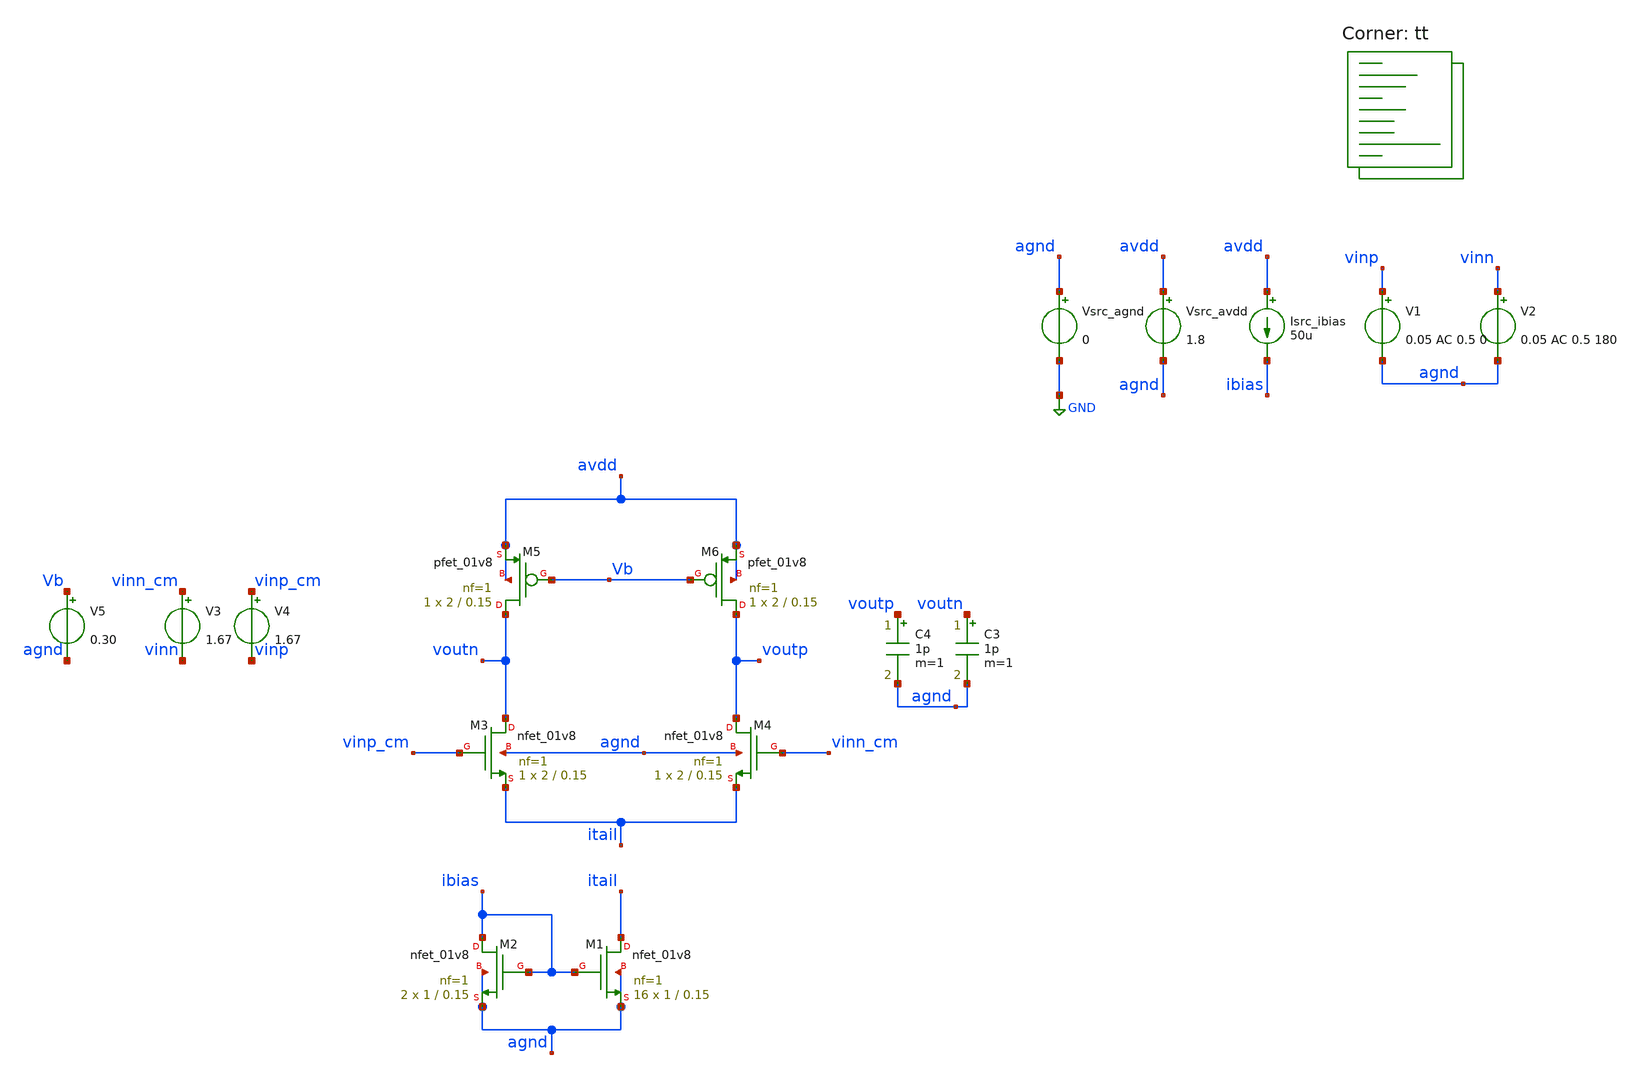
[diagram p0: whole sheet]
** sch_path: AMP/TB_Topologies_Diff.sch
**.subckt TB_Topologies_Diff
Vsrc_agnd agnd GND 0
Vsrc_avdd avdd agnd 1.8
Isrc_ibias avdd ibias 50u
V1 vinp agnd 0.05 AC 0.5 0
V2 vinn agnd 0.05 AC 0.5 180
C3 voutn agnd 1p m=1
C4 voutp agnd 1p m=1
XM1 itail ibias agnd agnd sky130_fd_pr__nfet_01v8 L=0.15 W=1 nf=1 ad='int((nf+1)/2) * W/nf * 0.29' as='int((nf+2)/2) * W/nf * 0.29'
+ pd='2*int((nf+1)/2) * (W/nf + 0.29)' ps='2*int((nf+2)/2) * (W/nf + 0.29)' nrd='0.29 / W' nrs='0.29 / W'
+ sa=0 sb=0 sd=0 mult=16 m=16
XM2 ibias ibias agnd agnd sky130_fd_pr__nfet_01v8 L=0.15 W=1 nf=1 ad='int((nf+1)/2) * W/nf * 0.29' as='int((nf+2)/2) * W/nf * 0.29'
+ pd='2*int((nf+1)/2) * (W/nf + 0.29)' ps='2*int((nf+2)/2) * (W/nf + 0.29)' nrd='0.29 / W' nrs='0.29 / W'
+ sa=0 sb=0 sd=0 mult=2 m=2
XM3 voutn vinp_cm itail agnd sky130_fd_pr__nfet_01v8 L=0.15 W=2 nf=1 ad='int((nf+1)/2) * W/nf * 0.29'
+ as='int((nf+2)/2) * W/nf * 0.29' pd='2*int((nf+1)/2) * (W/nf + 0.29)' ps='2*int((nf+2)/2) * (W/nf + 0.29)'
+ nrd='0.29 / W' nrs='0.29 / W' sa=0 sb=0 sd=0 mult=1 m=1
XM4 voutp vinn_cm itail agnd sky130_fd_pr__nfet_01v8 L=0.15 W=2 nf=1 ad='int((nf+1)/2) * W/nf * 0.29'
+ as='int((nf+2)/2) * W/nf * 0.29' pd='2*int((nf+1)/2) * (W/nf + 0.29)' ps='2*int((nf+2)/2) * (W/nf + 0.29)'
+ nrd='0.29 / W' nrs='0.29 / W' sa=0 sb=0 sd=0 mult=1 m=1
XM5 voutn Vb avdd avdd sky130_fd_pr__pfet_01v8 L=0.15 W=2 nf=1 ad='int((nf+1)/2) * W/nf * 0.29' as='int((nf+2)/2) * W/nf * 0.29'
+ pd='2*int((nf+1)/2) * (W/nf + 0.29)' ps='2*int((nf+2)/2) * (W/nf + 0.29)' nrd='0.29 / W' nrs='0.29 / W'
+ sa=0 sb=0 sd=0 mult=1 m=1
XM6 voutp Vb avdd avdd sky130_fd_pr__pfet_01v8 L=0.15 W=2 nf=1 ad='int((nf+1)/2) * W/nf * 0.29' as='int((nf+2)/2) * W/nf * 0.29'
+ pd='2*int((nf+1)/2) * (W/nf + 0.29)' ps='2*int((nf+2)/2) * (W/nf + 0.29)' nrd='0.29 / W' nrs='0.29 / W'
+ sa=0 sb=0 sd=0 mult=1 m=1
V3 vinn_cm vinn 1.67
V4 vinp_cm vinp 1.67
V5 Vb agnd 0.30
**** begin user architecture code

* this option enables mos model bin
* selection based on W/NF instead of W
.option wnflag=1

.option savecurrents

.control
save all
op

* Print newline
echo

* Store MOS lists
set nmos_list = ( xm1 xm2 xm3 xm4 )
set pmos_list = ( xm5 xm6 )
set nmos_lvt_list = (  )
set pmos_lvt_list = (  )

* Print stats for each MOSFET
foreach nmos $nmos_list
 * Save stats
 save @m.{$nmos}.msky130_fd_pr__nfet_01v8[gm]
 let vth   = @m.{$nmos}.msky130_fd_pr__nfet_01v8[vth]
 let vgs   = @m.{$nmos}.msky130_fd_pr__nfet_01v8[vgs]
 let vds   = @m.{$nmos}.msky130_fd_pr__nfet_01v8[vds]
 let vdsat = @m.{$nmos}.msky130_fd_pr__nfet_01v8[vdsat]
 let gm    = @m.{$nmos}.msky130_fd_pr__nfet_01v8[gm]
 let gds   = @m.{$nmos}.msky130_fd_pr__nfet_01v8[gds]


 * Print stats
 echo Stats for $nmos:
 print vth
 print vgs
 print vds
 print vdsat
 print gm
 print gds

 * Print newline
 echo
end

foreach pmos $pmos_list
 * Save stats
 save @m.{$pmos}.msky130_fd_pr__nfet_01v8[gm]
 let vth   = @m.{$pmos}.msky130_fd_pr__pfet_01v8[vth]
 let vgs   = @m.{$pmos}.msky130_fd_pr__pfet_01v8[vgs]
 let vds   = @m.{$pmos}.msky130_fd_pr__pfet_01v8[vds]
 let vdsat = @m.{$pmos}.msky130_fd_pr__pfet_01v8[vdsat]
 let gm    = @m.{$pmos}.msky130_fd_pr__pfet_01v8[gm]
 let gds   = @m.{$pmos}.msky130_fd_pr__pfet_01v8[gds]

 * Print stats
 echo Stats for $pmos:
 print vth
 print vgs
 print vds
 print vdsat
 print gm
 print gds

 * Print newline
 echo
end

foreach nmos_lvt $nmos_lvt_list
 * Save stats
 save @m.{$nmos_lvt}.msky130_fd_pr__nfet_01v8_lvt[gm]
 let vth   = @m.{$nmos_lvt}.msky130_fd_pr__nfet_01v8_lvt[vth]
 let vgs   = @m.{$nmos_lvt}.msky130_fd_pr__nfet_01v8_lvt[vgs]
 let vds   = @m.{$nmos_lvt}.msky130_fd_pr__nfet_01v8_lvt[vds]
 let vdsat = @m.{$nmos_lvt}.msky130_fd_pr__nfet_01v8_lvt[vdsat]
 let gm    = @m.{$nmos_lvt}.msky130_fd_pr__nfet_01v8_lvt[gm]
 let gds   = @m.{$nmos_lvt}.msky130_fd_pr__nfet_01v8_lvt[gds]


 * Print stats
 echo Stats for $nmos_lvt:
 print vth
 print vgs
 print vds
 print vdsat
 print gm
 print gds

 * Print newline
 echo
end

foreach pmos_lvt $pmos_lvt_list
 * Save stats
 save @m.{$pmos_lvt}.msky130_fd_pr__nfet_01v8_lvt[gm]
 let vth   = @m.{$pmos_lvt}.msky130_fd_pr__pfet_01v8_lvt[vth]
 let vgs   = @m.{$pmos_lvt}.msky130_fd_pr__pfet_01v8_lvt[vgs]
 let vds   = @m.{$pmos_lvt}.msky130_fd_pr__pfet_01v8_lvt[vds]
 let vdsat = @m.{$pmos_lvt}.msky130_fd_pr__pfet_01v8_lvt[vdsat]
 let gm    = @m.{$pmos_lvt}.msky130_fd_pr__pfet_01v8_lvt[gm]
 let gds   = @m.{$pmos_lvt}.msky130_fd_pr__pfet_01v8_lvt[gds]


 * Print stats
 echo Stats for $pmos_lvt:
 print vth
 print vgs
 print vds
 print vdsat
 print gm
 print gds

 * Print newline
 echo
end

* Print region of operation
echo Regions of Operation:
echo

echo NMOS:
foreach nmos $nmos_list
 * Save stats
 let vds = @m.{$nmos}.msky130_fd_pr__nfet_01v8[vds]
 let vgs = @m.{$nmos}.msky130_fd_pr__nfet_01v8[vgs]
 let vth = @m.{$nmos}.msky130_fd_pr__nfet_01v8[vth]

 * Check and print regions
 if (vgs <= vth)
  echo $nmos: N Cutoff
  print vgs
  print vth
 end
 if (vgs > vth) & (vds <= (vgs - vth))
  echo $nmos: N Triode
  print vgs
  print vth
  print vds
 end
 if (vgs > vth) & (vds > (vgs - vth))
  echo $nmos: N Saturation
 end
end
echo

echo PMOS:
foreach pmos $pmos_list
 * Save stats
 let vds = @m.{$pmos}.msky130_fd_pr__pfet_01v8[vds]
 let vgs = @m.{$pmos}.msky130_fd_pr__pfet_01v8[vgs]
 let vth = @m.{$pmos}.msky130_fd_pr__pfet_01v8[vth]

 * Check and print regions
 if (abs(vgs) <= abs(vth))
  echo $pmos: P Cutoff
  print vgs
  print vth
 end
 if (abs(vgs) > abs(vth)) & (abs(vds) <= (abs(vgs) - abs(vth)))
  echo $pmos: P Triode
  print vgs
  print vth
  print vds
 end
 if (abs(vgs) > abs(vth)) & (abs(vds) > (abs(vgs) - abs(vth)))
  echo $pmos: P Saturation
 end
end
echo

echo NMOS_lvt:
foreach nmos_lvt $nmos_lvt_list
 * Save stats
 let vds = @m.{$nmos_lvt}.msky130_fd_pr__nfet_01v8_lvt[vds]
 let vgs = @m.{$nmos_lvt}.msky130_fd_pr__nfet_01v8_lvt[vgs]
 let vth = @m.{$nmos_lvt}.msky130_fd_pr__nfet_01v8_lvt[vth]

 * Check and print regions
 if (vgs <= vth)
  echo $nmos_lvt: N Cutoff
  print vgs
  print vth
 end
 if (vgs > vth) & (vds <= (vgs - vth))
  echo $nmos_lvt: N Triode
  print vgs
  print vth
  print vds
 end
 if (vgs > vth) & (vds > (vgs - vth))
  echo $nmos_lvt: N Saturation
 end
end
echo

echo PMOS_lvt:
foreach pmos_lvt $pmos_lvt_list
 * Save stats
 let vds = @m.{$pmos_lvt}.msky130_fd_pr__pfet_01v8_lvt[vds]
 let vgs = @m.{$pmos_lvt}.msky130_fd_pr__pfet_01v8_lvt[vgs]
 let vth = @m.{$pmos_lvt}.msky130_fd_pr__pfet_01v8_lvt[vth]

 * Check and print regions
 if (abs(vgs) <= abs(vth))
  echo $pmos_lvt: P Cutoff
  print vgs
  print vth
 end
 if (abs(vgs) > abs(vth)) & (abs(vds) <= (abs(vgs) - abs(vth)))
  echo $pmos_lvt: P Triode
  print vgs
  print vth
  print vds
 end
 if (abs(vgs) > abs(vth)) & (abs(vds) > (abs(vgs) - abs(vth)))
  echo $pmos_lvt: P Saturation
 end
end
echo

* Sweep frequency
write TB_Topologies_Diff.raw
set appendwrite
ac dec 100 1e0 1e11
remzerovec

* Calculate gain
let vout_diff = v(voutp)- v(voutn)
let vin_diff = v(vinp)- v(vinn)
let gain_00 = db(mag(vout_diff/vin_diff))
let ratio_00 = (vout_diff/vin_diff)

write TB_Topologies_Diff.raw

.endc


.lib $::SKYWATER_MODELS/sky130.lib.spice tt
**** end user architecture code
**.ends
.GLOBAL GND
.end
